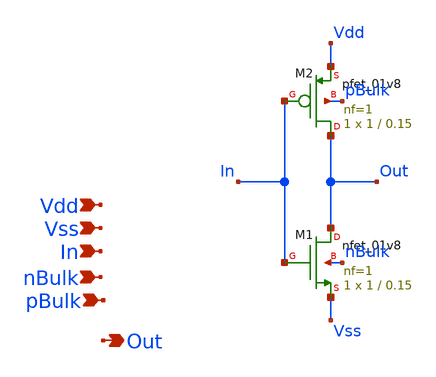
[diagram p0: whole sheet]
** sch_path: tt10-hdl/tt_um_test_commit/xschem/T0/inv/inv.sch
**.subckt inv Vdd Vss Out In nBulk pBulk
*.ipin Vdd
*.ipin Vss
*.opin Out
*.ipin In
*.ipin nBulk
*.ipin pBulk
XM1 Out In Vss nBulk sky130_fd_pr__nfet_01v8 L=0.15 W=1 nf=1 ad='int((1 + 1)/2) * 1 / 1 * 0.29' as='int((1 + 2)/2) * 1 / 1 * 0.29'
+ pd='2*int((1 + 1)/2) * (1 / 1 + 0.29)' ps='2*int((1 + 2)/2) * (1 / 1 + 0.29)' nrd='0.29 / 1 ' nrs='0.29 / 1 '
+ sa=0 sb=0 sd=0 mult=1 m=1
XM2 Out In Vdd pBulk sky130_fd_pr__pfet_01v8 L=0.15 W=1 nf=1 ad='int((nf+1)/2) * W/nf * 0.29' as='int((nf+2)/2) * W/nf * 0.29'
+ pd='2*int((nf+1)/2) * (W/nf + 0.29)' ps='2*int((nf+2)/2) * (W/nf + 0.29)' nrd='0.29 / W' nrs='0.29 / W'
+ sa=0 sb=0 sd=0 mult=1 m=1
**.ends
.end
